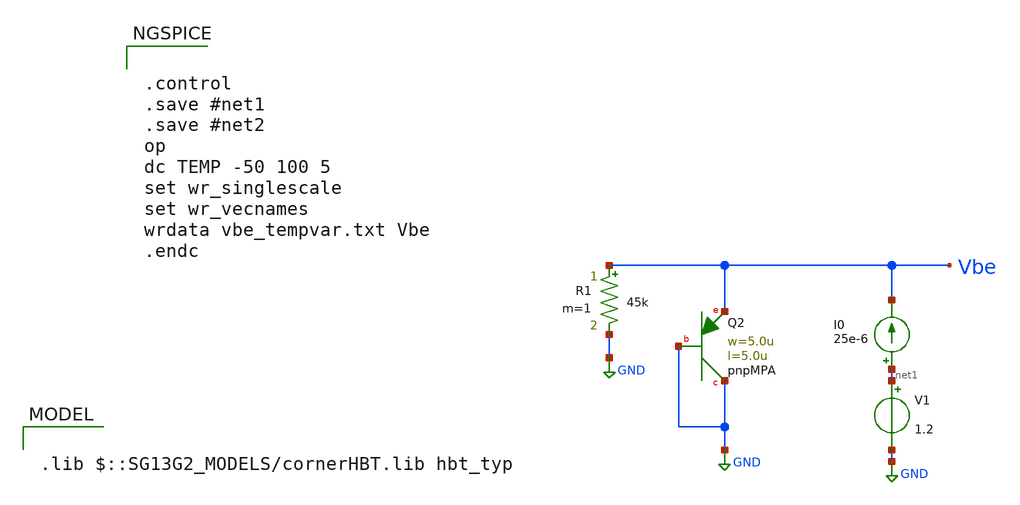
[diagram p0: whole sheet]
** sch_path: modules/module_1_bandgap_reference/part_2_full_bgr/schematic/vbesim.sch
**.subckt vbesim
R1 Vbe GND 45k m=1
I0 net1 Vbe 25e-6
XQ2 GND GND Vbe pnpMPA a=25p p=20u m=1
V1 net1 GND 1.2
**** begin user architecture code


.control
.save #net1
.save #net2
op
dc TEMP -50 100 5
set wr_singlescale
set wr_vecnames
wrdata vbe_tempvar.txt Vbe
.endc




.lib $::SG13G2_MODELS/cornerHBT.lib hbt_typ

**** end user architecture code
**.ends
.GLOBAL GND
.end
